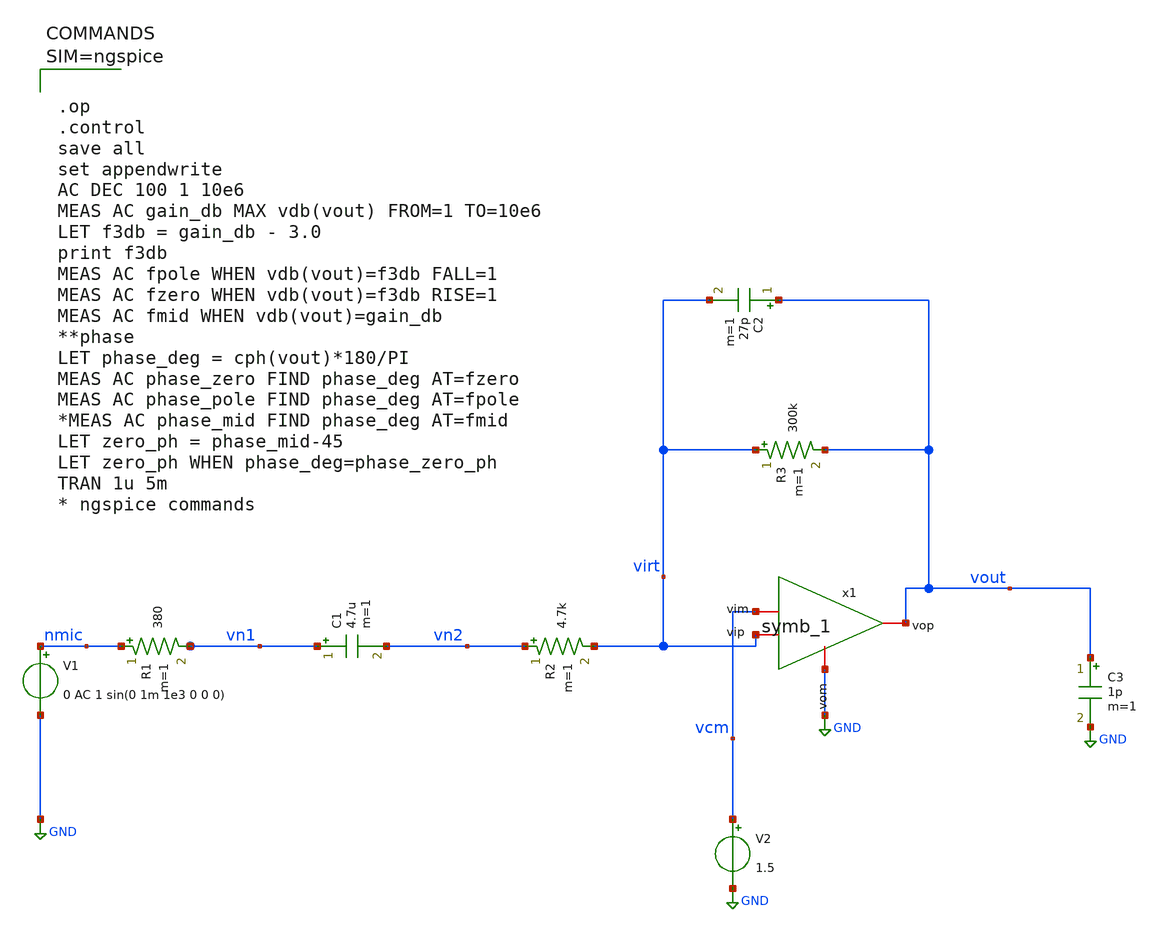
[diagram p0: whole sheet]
** sch_path: xschem/main_opa.sch
**.subckt main_opa
V1 nmic GND 0 AC 1 sin(0 1m 1e3 0 0 0)
R1 nmic vn1 380 m=1
C1 vn1 vn2 4.7u m=1
R2 vn2 virt 4.7k m=1
R3 virt vout 300k m=1
C2 vout virt 27p m=1
V2 vcm GND 1.5
C3 vout GND 1p m=1
x1 vout virt vcm GND symb_1
**** begin user architecture code



.op
.control
save all
set appendwrite
AC DEC 100 1 10e6
MEAS AC gain_db MAX vdb(vout) FROM=1 TO=10e6
LET f3db = gain_db - 3.0
print f3db
MEAS AC fpole WHEN vdb(vout)=f3db FALL=1
MEAS AC fzero WHEN vdb(vout)=f3db RISE=1
MEAS AC fmid WHEN vdb(vout)=gain_db
**phase
LET phase_deg = cph(vout)*180/PI
MEAS AC phase_zero FIND phase_deg AT=fzero
MEAS AC phase_pole FIND phase_deg AT=fpole
*MEAS AC phase_mid FIND phase_deg AT=fmid
LET zero_ph = phase_mid-45
LET zero_ph WHEN phase_deg=phase_zero_ph
TRAN 1u 5m
* ngspice commands



**** end user architecture code
**.ends

* expanding   symbol:  symb_1.sym # of pins=4
** sym_path: xschem/symb_1.sym
** sch_path: xschem/symb_1.sch
.subckt symb_1 vop vip vim vom
*.iopin vip
*.iopin vim
*.iopin vop
*.iopin vom
E1 vop vom vip vim 3
.ends

.GLOBAL GND
.end
